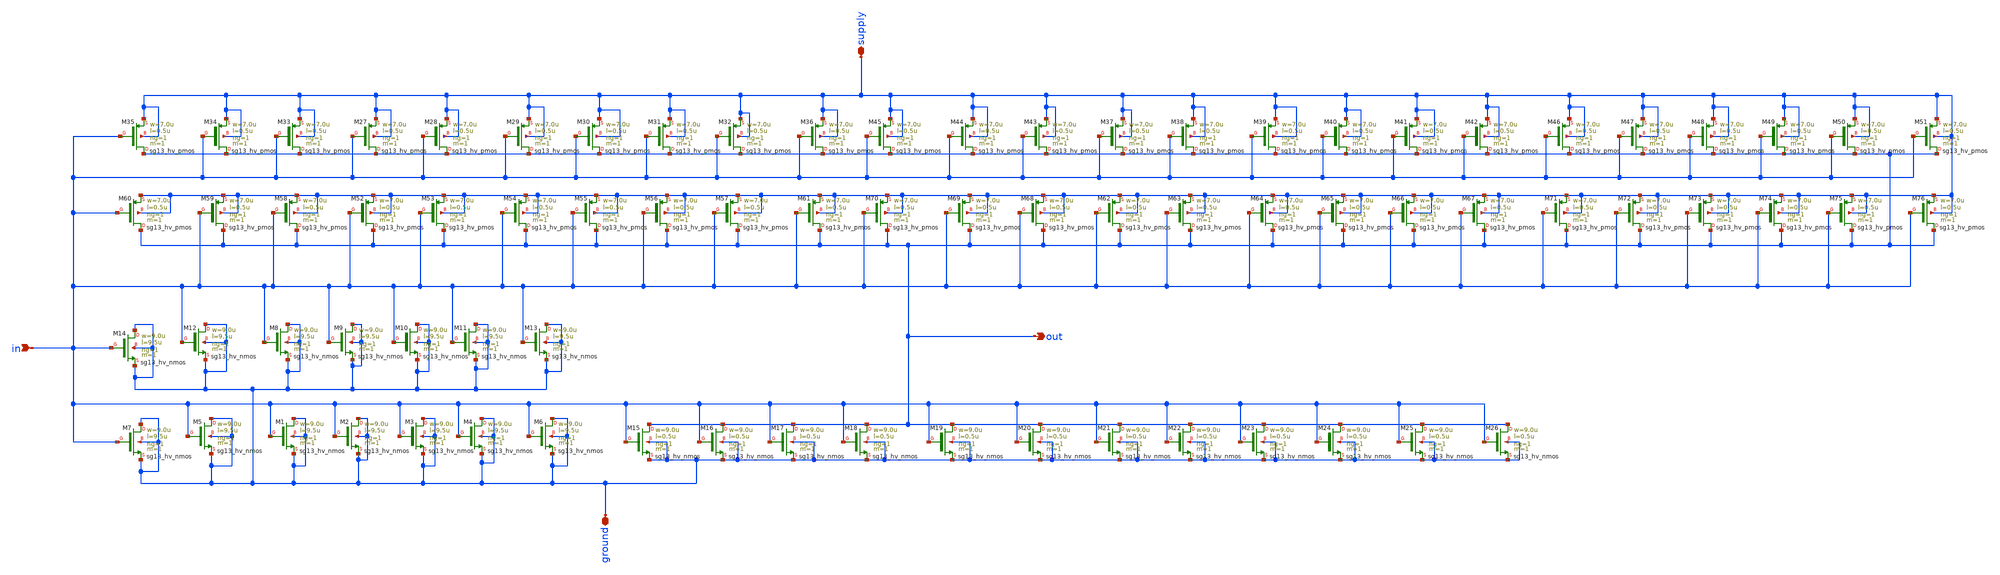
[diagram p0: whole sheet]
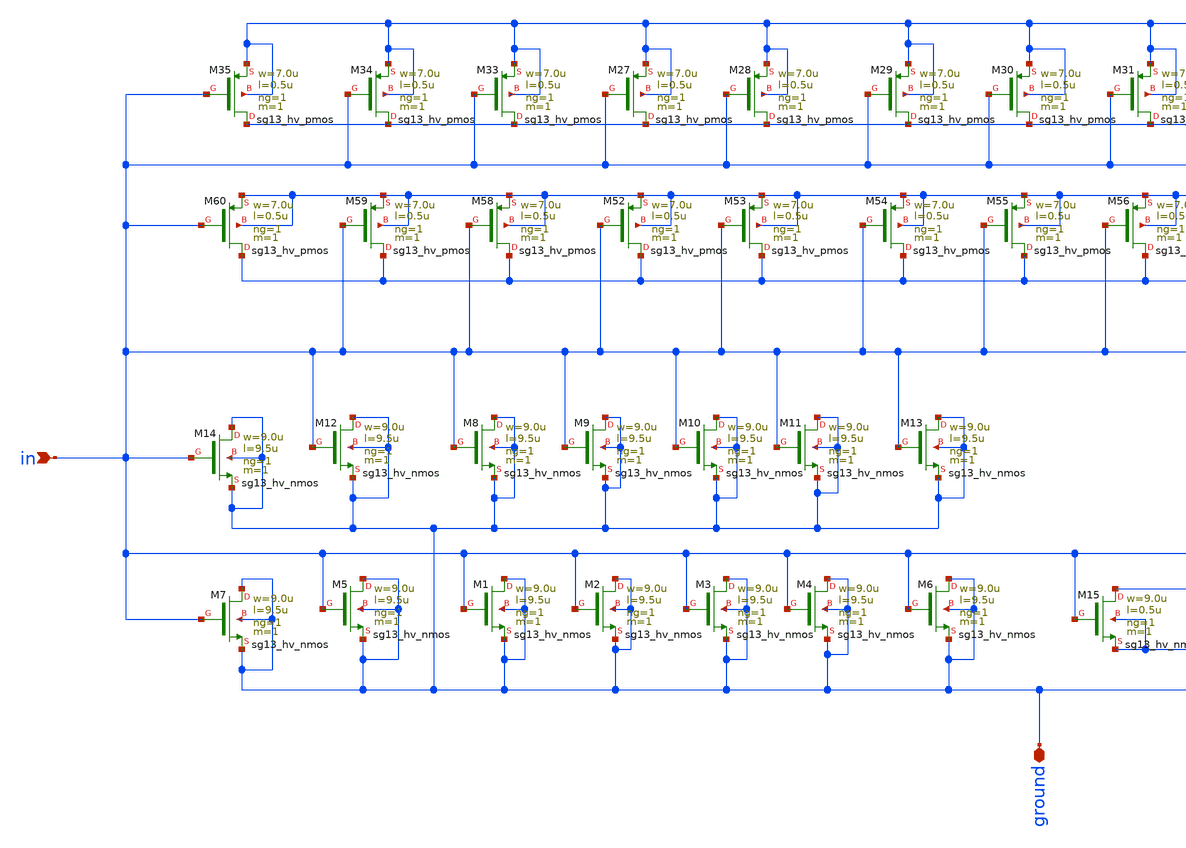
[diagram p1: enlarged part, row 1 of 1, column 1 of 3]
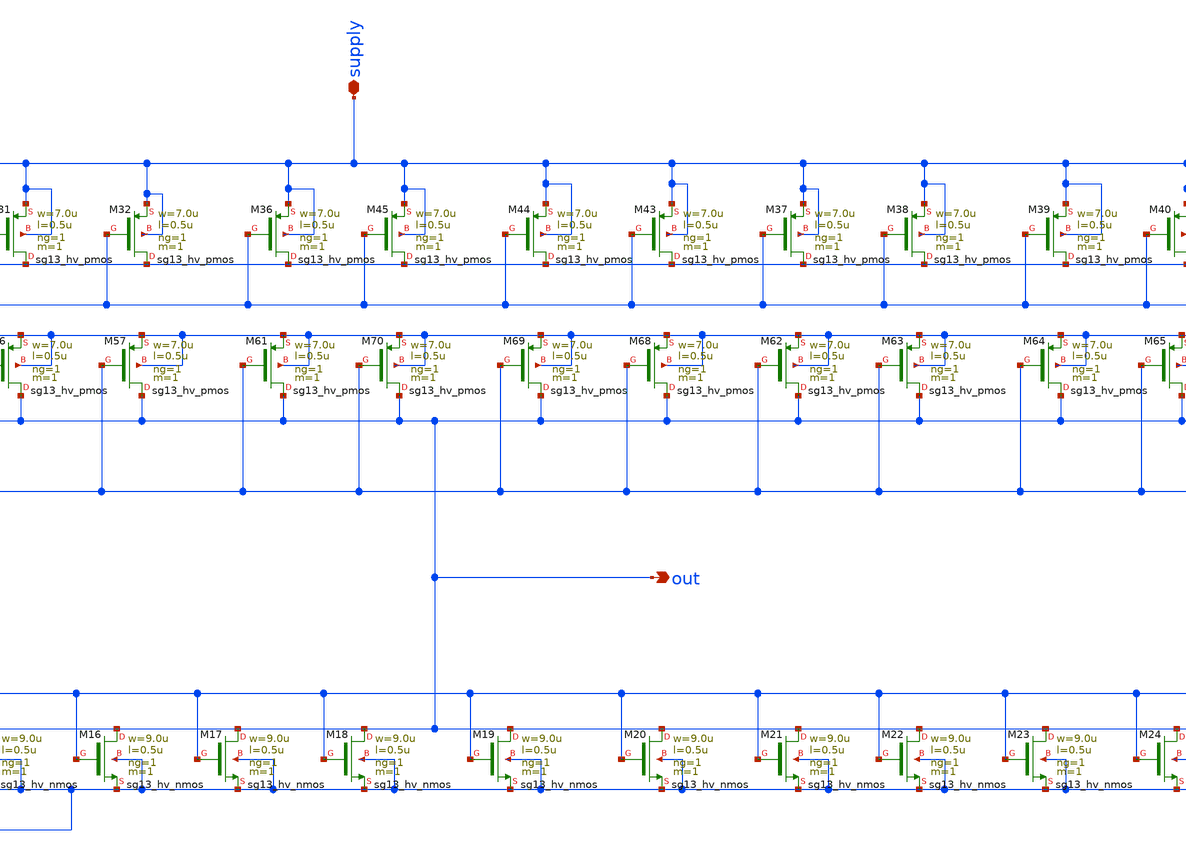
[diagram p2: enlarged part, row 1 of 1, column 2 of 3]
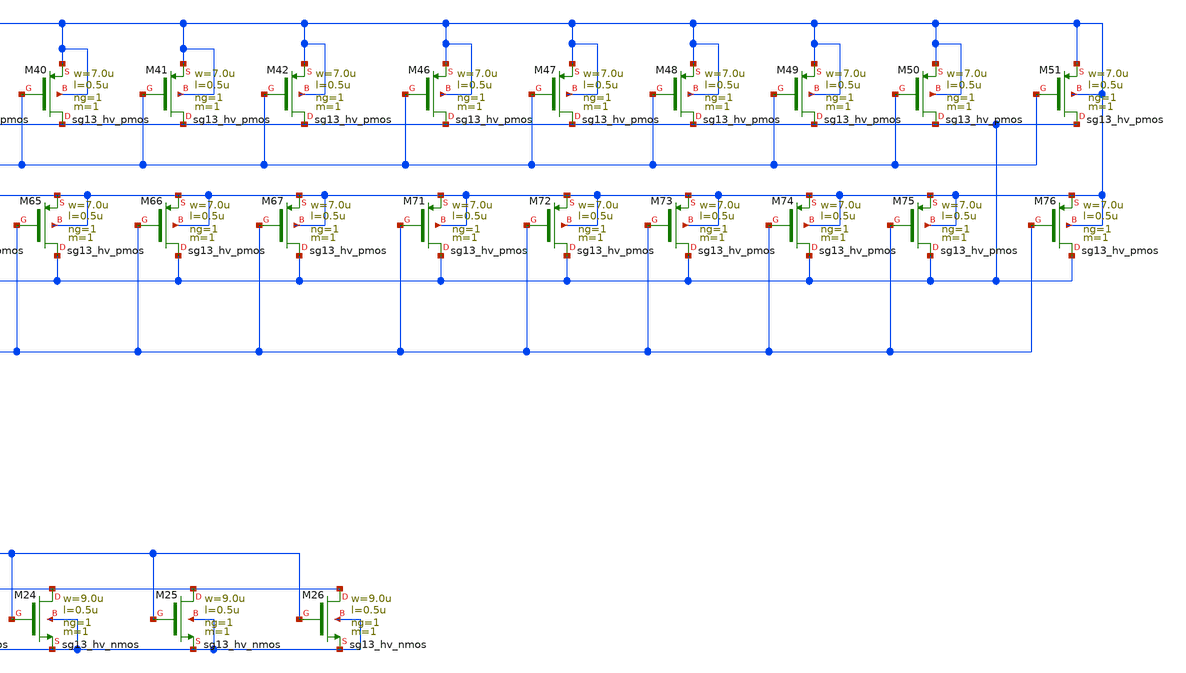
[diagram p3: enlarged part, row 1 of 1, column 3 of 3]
** sch_path: OTA_Telescopic_v3/Schematics_and_Symbols/IOCells/sg13g2_RCClampInverter.sch
**.subckt sg13g2_RCClampInverter supply ground out in
*.iopin supply
*.iopin ground
*.opin out
*.ipin in
XM1 ground in ground ground sg13_hv_nmos w=9.0u l=9.5u ng=1 m=1 mm_ok=1
XM2 ground in ground ground sg13_hv_nmos w=9.0u l=9.5u ng=1 m=1 mm_ok=1
XM3 ground in ground ground sg13_hv_nmos w=9.0u l=9.5u ng=1 m=1 mm_ok=1
XM4 ground in ground ground sg13_hv_nmos w=9.0u l=9.5u ng=1 m=1 mm_ok=1
XM5 ground in ground ground sg13_hv_nmos w=9.0u l=9.5u ng=1 m=1 mm_ok=1
XM6 ground in ground ground sg13_hv_nmos w=9.0u l=9.5u ng=1 m=1 mm_ok=1
XM7 ground in ground ground sg13_hv_nmos w=9.0u l=9.5u ng=1 m=1 mm_ok=1
XM8 ground in ground ground sg13_hv_nmos w=9.0u l=9.5u ng=1 m=1 mm_ok=1
XM9 ground in ground ground sg13_hv_nmos w=9.0u l=9.5u ng=1 m=1 mm_ok=1
XM10 ground in ground ground sg13_hv_nmos w=9.0u l=9.5u ng=1 m=1 mm_ok=1
XM11 ground in ground ground sg13_hv_nmos w=9.0u l=9.5u ng=1 m=1 mm_ok=1
XM12 ground in ground ground sg13_hv_nmos w=9.0u l=9.5u ng=1 m=1 mm_ok=1
XM13 ground in ground ground sg13_hv_nmos w=9.0u l=9.5u ng=1 m=1 mm_ok=1
XM14 ground in ground ground sg13_hv_nmos w=9.0u l=9.5u ng=1 m=1 mm_ok=1
XM15 out in ground ground sg13_hv_nmos w=9.0u l=0.5u ng=1 m=1 mm_ok=1
XM16 out in ground ground sg13_hv_nmos w=9.0u l=0.5u ng=1 m=1 mm_ok=1
XM17 out in ground ground sg13_hv_nmos w=9.0u l=0.5u ng=1 m=1 mm_ok=1
XM18 out in ground ground sg13_hv_nmos w=9.0u l=0.5u ng=1 m=1 mm_ok=1
XM19 out in ground ground sg13_hv_nmos w=9.0u l=0.5u ng=1 m=1 mm_ok=1
XM20 out in ground ground sg13_hv_nmos w=9.0u l=0.5u ng=1 m=1 mm_ok=1
XM21 out in ground ground sg13_hv_nmos w=9.0u l=0.5u ng=1 m=1 mm_ok=1
XM22 out in ground ground sg13_hv_nmos w=9.0u l=0.5u ng=1 m=1 mm_ok=1
XM23 out in ground ground sg13_hv_nmos w=9.0u l=0.5u ng=1 m=1 mm_ok=1
XM24 out in ground ground sg13_hv_nmos w=9.0u l=0.5u ng=1 m=1 mm_ok=1
XM25 out in ground ground sg13_hv_nmos w=9.0u l=0.5u ng=1 m=1 mm_ok=1
XM26 out in ground ground sg13_hv_nmos w=9.0u l=0.5u ng=1 m=1 mm_ok=1
XM27 out in supply supply sg13_hv_pmos w=7.0u l=0.5u ng=1 m=1 mm_ok=1
XM28 out in supply supply sg13_hv_pmos w=7.0u l=0.5u ng=1 m=1 mm_ok=1
XM29 out in supply supply sg13_hv_pmos w=7.0u l=0.5u ng=1 m=1 mm_ok=1
XM30 out in supply supply sg13_hv_pmos w=7.0u l=0.5u ng=1 m=1 mm_ok=1
XM31 out in supply supply sg13_hv_pmos w=7.0u l=0.5u ng=1 m=1 mm_ok=1
XM32 out in supply supply sg13_hv_pmos w=7.0u l=0.5u ng=1 m=1 mm_ok=1
XM33 out in supply supply sg13_hv_pmos w=7.0u l=0.5u ng=1 m=1 mm_ok=1
XM34 out in supply supply sg13_hv_pmos w=7.0u l=0.5u ng=1 m=1 mm_ok=1
XM35 out in supply supply sg13_hv_pmos w=7.0u l=0.5u ng=1 m=1 mm_ok=1
XM36 out in supply supply sg13_hv_pmos w=7.0u l=0.5u ng=1 m=1 mm_ok=1
XM37 out in supply supply sg13_hv_pmos w=7.0u l=0.5u ng=1 m=1 mm_ok=1
XM38 out in supply supply sg13_hv_pmos w=7.0u l=0.5u ng=1 m=1 mm_ok=1
XM39 out in supply supply sg13_hv_pmos w=7.0u l=0.5u ng=1 m=1 mm_ok=1
XM40 out in supply supply sg13_hv_pmos w=7.0u l=0.5u ng=1 m=1 mm_ok=1
XM41 out in supply supply sg13_hv_pmos w=7.0u l=0.5u ng=1 m=1 mm_ok=1
XM42 out in supply supply sg13_hv_pmos w=7.0u l=0.5u ng=1 m=1 mm_ok=1
XM43 out in supply supply sg13_hv_pmos w=7.0u l=0.5u ng=1 m=1 mm_ok=1
XM44 out in supply supply sg13_hv_pmos w=7.0u l=0.5u ng=1 m=1 mm_ok=1
XM45 out in supply supply sg13_hv_pmos w=7.0u l=0.5u ng=1 m=1 mm_ok=1
XM46 out in supply supply sg13_hv_pmos w=7.0u l=0.5u ng=1 m=1 mm_ok=1
XM47 out in supply supply sg13_hv_pmos w=7.0u l=0.5u ng=1 m=1 mm_ok=1
XM48 out in supply supply sg13_hv_pmos w=7.0u l=0.5u ng=1 m=1 mm_ok=1
XM49 out in supply supply sg13_hv_pmos w=7.0u l=0.5u ng=1 m=1 mm_ok=1
XM50 out in supply supply sg13_hv_pmos w=7.0u l=0.5u ng=1 m=1 mm_ok=1
XM51 out in supply supply sg13_hv_pmos w=7.0u l=0.5u ng=1 m=1 mm_ok=1
XM52 out in supply supply sg13_hv_pmos w=7.0u l=0.5u ng=1 m=1 mm_ok=1
XM53 out in supply supply sg13_hv_pmos w=7.0u l=0.5u ng=1 m=1 mm_ok=1
XM54 out in supply supply sg13_hv_pmos w=7.0u l=0.5u ng=1 m=1 mm_ok=1
XM55 out in supply supply sg13_hv_pmos w=7.0u l=0.5u ng=1 m=1 mm_ok=1
XM56 out in supply supply sg13_hv_pmos w=7.0u l=0.5u ng=1 m=1 mm_ok=1
XM57 out in supply supply sg13_hv_pmos w=7.0u l=0.5u ng=1 m=1 mm_ok=1
XM58 out in supply supply sg13_hv_pmos w=7.0u l=0.5u ng=1 m=1 mm_ok=1
XM59 out in supply supply sg13_hv_pmos w=7.0u l=0.5u ng=1 m=1 mm_ok=1
XM60 out in supply supply sg13_hv_pmos w=7.0u l=0.5u ng=1 m=1 mm_ok=1
XM61 out in supply supply sg13_hv_pmos w=7.0u l=0.5u ng=1 m=1 mm_ok=1
XM62 out in supply supply sg13_hv_pmos w=7.0u l=0.5u ng=1 m=1 mm_ok=1
XM63 out in supply supply sg13_hv_pmos w=7.0u l=0.5u ng=1 m=1 mm_ok=1
XM64 out in supply supply sg13_hv_pmos w=7.0u l=0.5u ng=1 m=1 mm_ok=1
XM65 out in supply supply sg13_hv_pmos w=7.0u l=0.5u ng=1 m=1 mm_ok=1
XM66 out in supply supply sg13_hv_pmos w=7.0u l=0.5u ng=1 m=1 mm_ok=1
XM67 out in supply supply sg13_hv_pmos w=7.0u l=0.5u ng=1 m=1 mm_ok=1
XM68 out in supply supply sg13_hv_pmos w=7.0u l=0.5u ng=1 m=1 mm_ok=1
XM69 out in supply supply sg13_hv_pmos w=7.0u l=0.5u ng=1 m=1 mm_ok=1
XM70 out in supply supply sg13_hv_pmos w=7.0u l=0.5u ng=1 m=1 mm_ok=1
XM71 out in supply supply sg13_hv_pmos w=7.0u l=0.5u ng=1 m=1 mm_ok=1
XM72 out in supply supply sg13_hv_pmos w=7.0u l=0.5u ng=1 m=1 mm_ok=1
XM73 out in supply supply sg13_hv_pmos w=7.0u l=0.5u ng=1 m=1 mm_ok=1
XM74 out in supply supply sg13_hv_pmos w=7.0u l=0.5u ng=1 m=1 mm_ok=1
XM75 out in supply supply sg13_hv_pmos w=7.0u l=0.5u ng=1 m=1 mm_ok=1
XM76 out in supply supply sg13_hv_pmos w=7.0u l=0.5u ng=1 m=1 mm_ok=1
**.ends
.end
